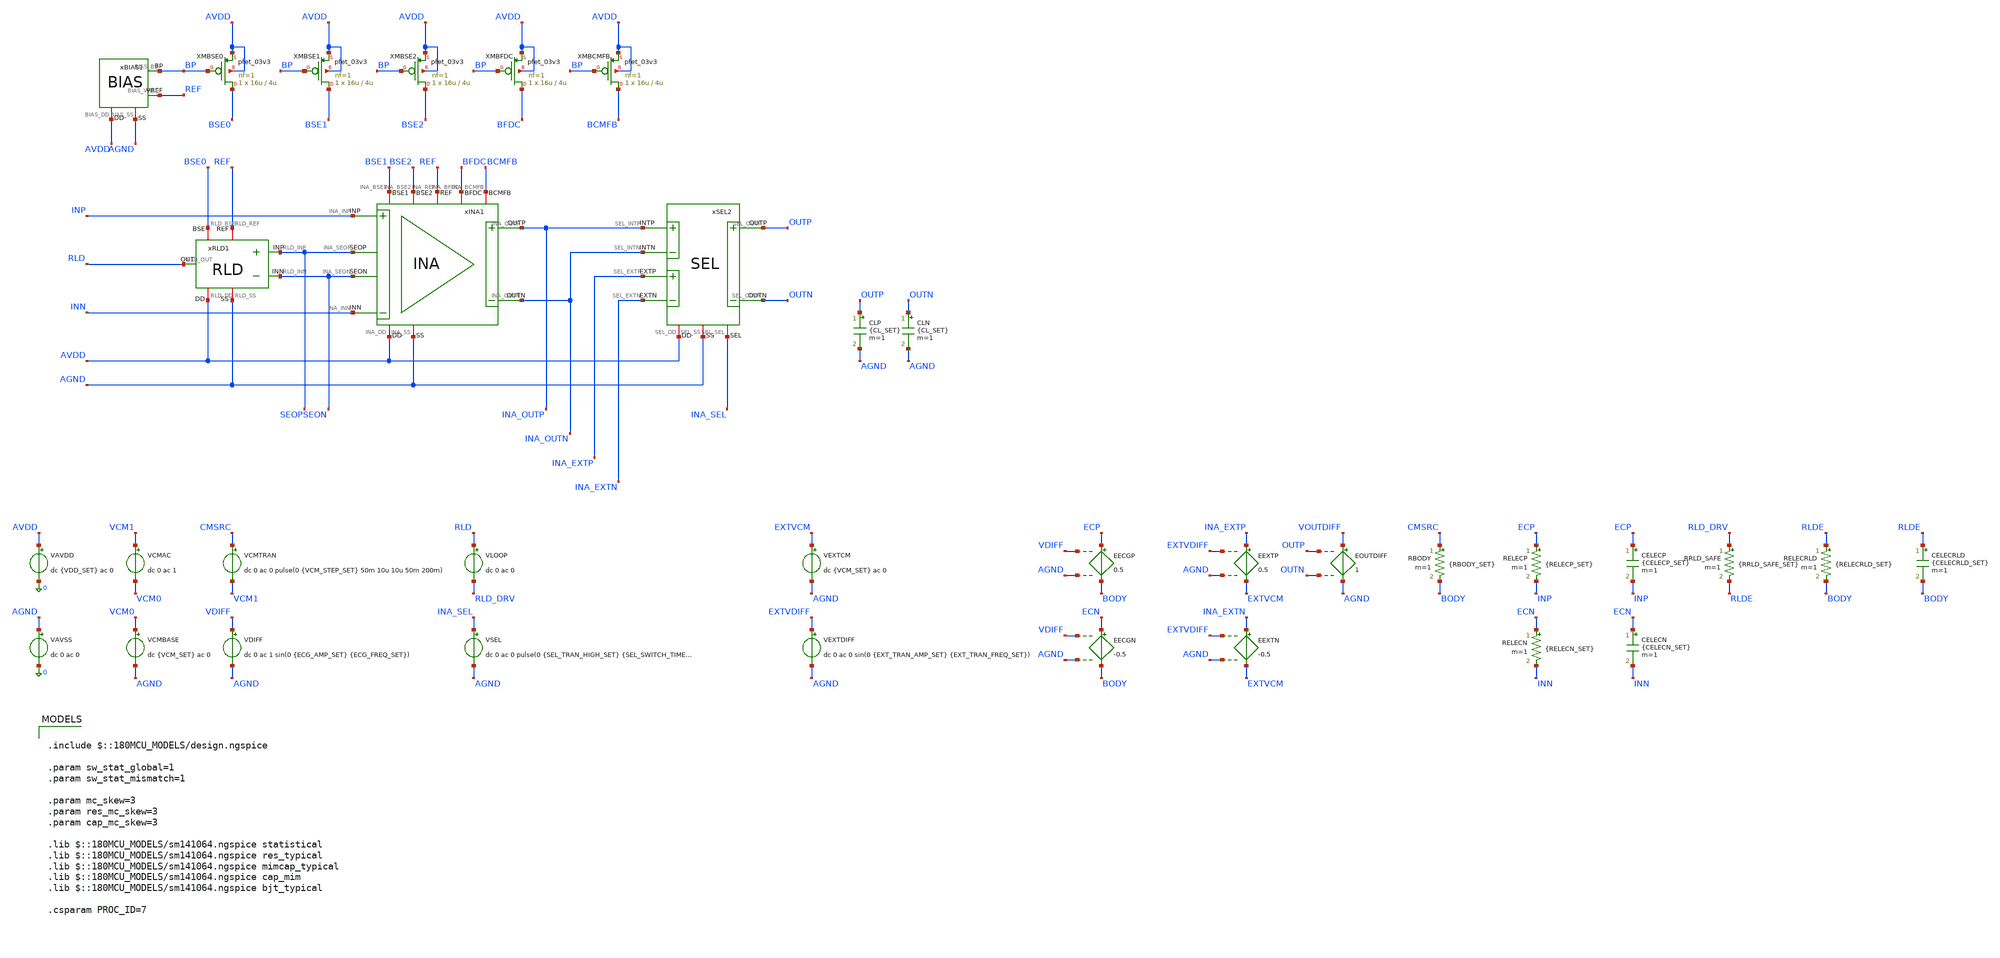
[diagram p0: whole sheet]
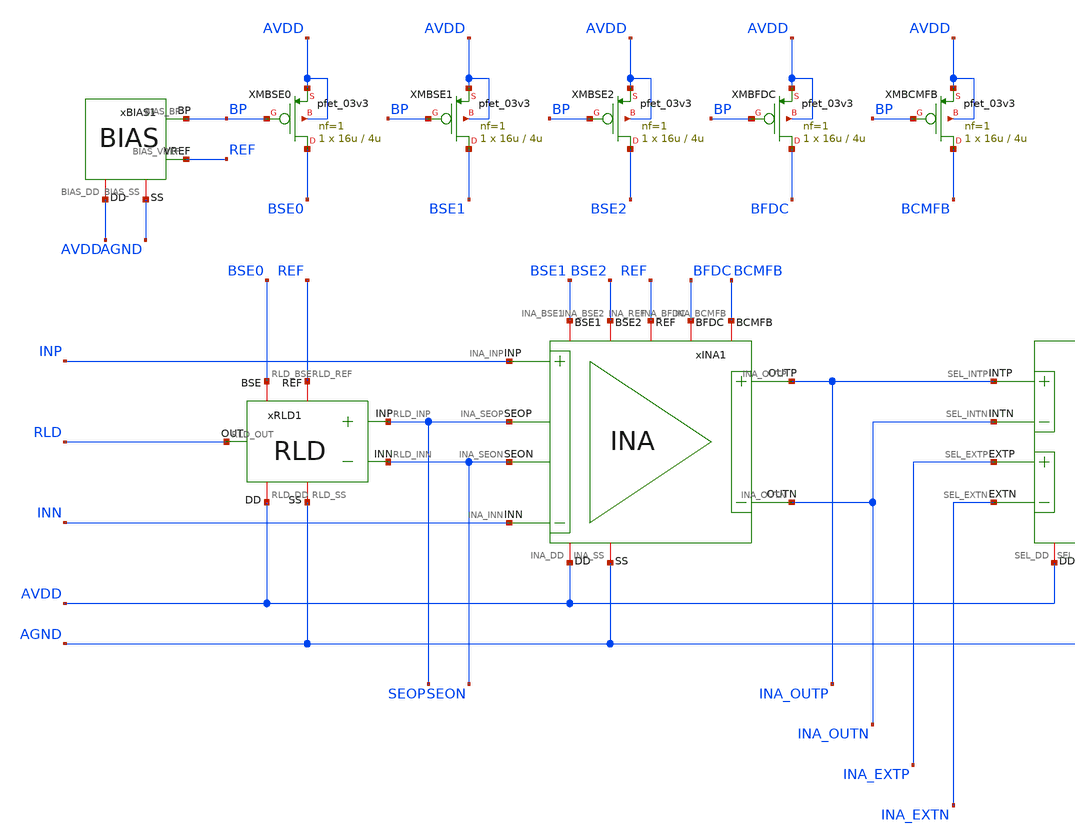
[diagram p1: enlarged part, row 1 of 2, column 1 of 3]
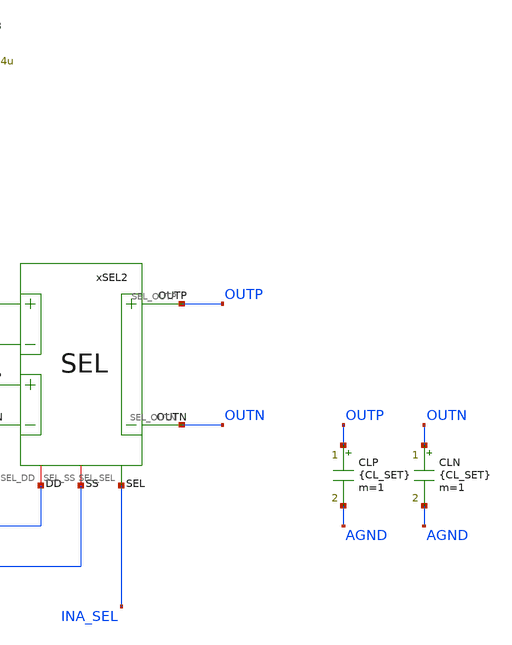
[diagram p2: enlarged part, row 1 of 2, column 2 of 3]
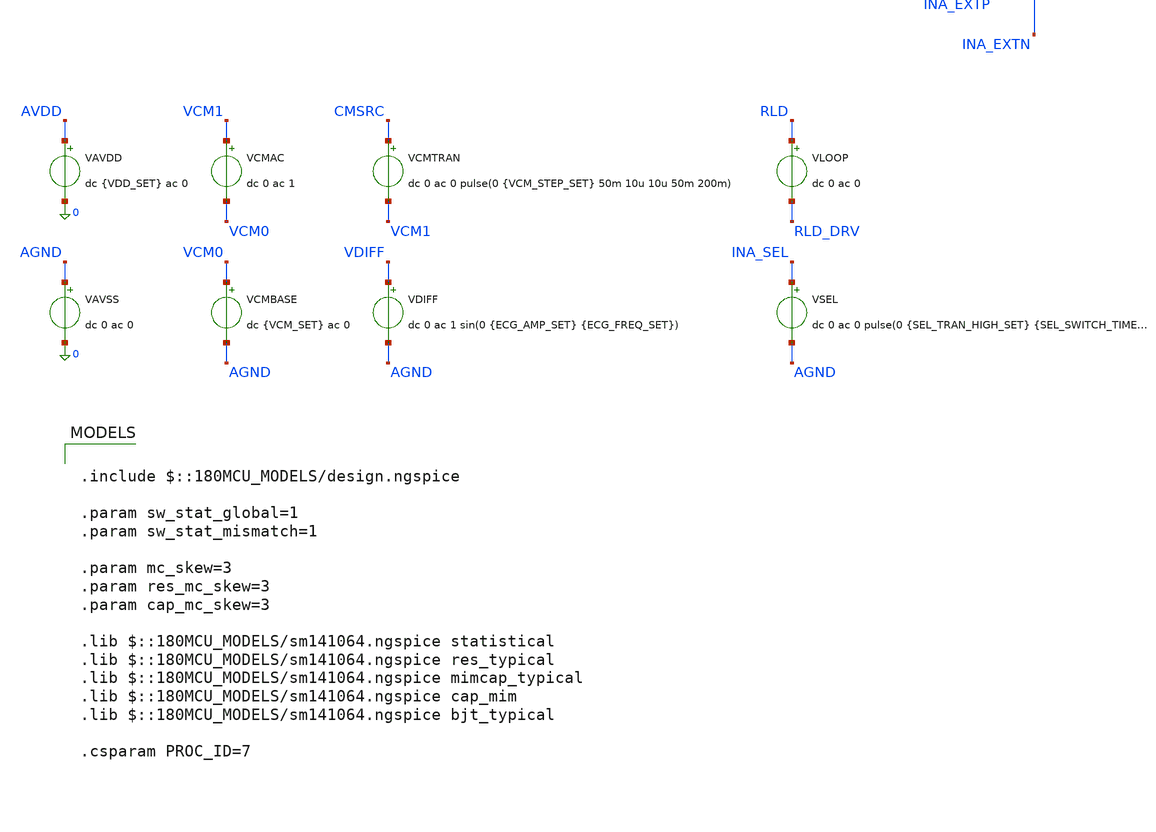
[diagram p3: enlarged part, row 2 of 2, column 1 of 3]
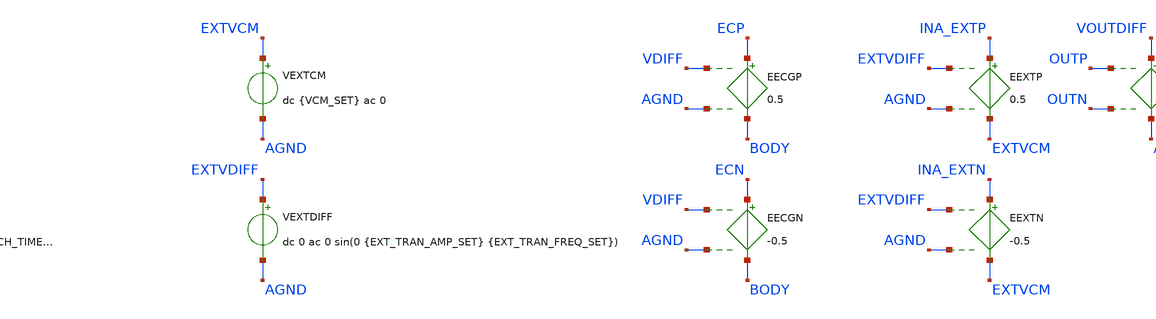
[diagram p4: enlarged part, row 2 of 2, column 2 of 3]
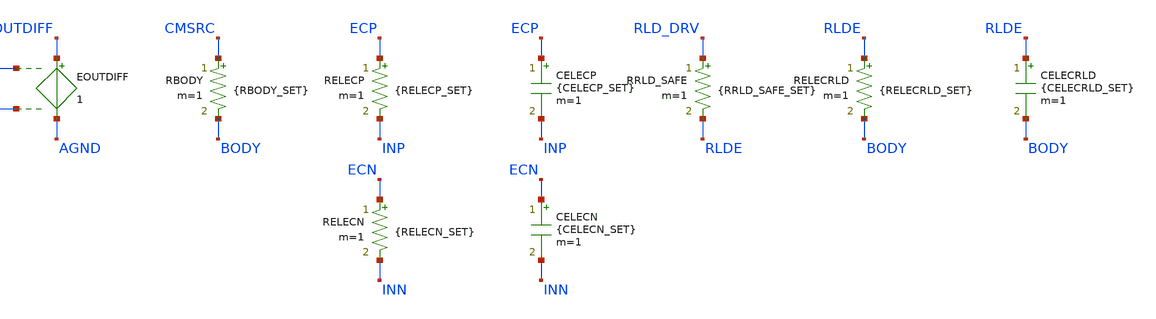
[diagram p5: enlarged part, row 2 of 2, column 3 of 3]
** sch_path: Design_Files/IC Design/Testbench/INA_RLD/INA_RLD_TB_FULL.sch
**.subckt INA_RLD_TB_FULL
xSEL2 AVDD AGND INA_OUTP INA_OUTN OUTN OUTP INA_EXTP INA_EXTN INA_SEL SEL
xINA1 AVDD AGND INP INN INA_OUTN BFDC INA_OUTP BCMFB REF SEON SEOP BSE1 BSE2 INA
xRLD1 AVDD AGND SEOP SEON RLD REF BSE0 RLD
CLP OUTP AGND {CL_SET} m=1
CLN OUTN AGND {CL_SET} m=1
xBIAS1 AVDD AGND BP REF BIAS
XMBSE0 BSE0 BP AVDD AVDD pfet_03v3 L=4u W=16u nf=1 ad='int((nf+1)/2) * W/nf * 0.18u' as='int((nf+2)/2) * W/nf * 0.18u'
+ pd='2*int((nf+1)/2) * (W/nf + 0.18u)' ps='2*int((nf+2)/2) * (W/nf + 0.18u)' nrd='0.18u / W' nrs='0.18u / W'
+ sa=0 sb=0 sd=0 m=1
XMBSE1 BSE1 BP AVDD AVDD pfet_03v3 L=4u W=16u nf=1 ad='int((nf+1)/2) * W/nf * 0.18u' as='int((nf+2)/2) * W/nf * 0.18u'
+ pd='2*int((nf+1)/2) * (W/nf + 0.18u)' ps='2*int((nf+2)/2) * (W/nf + 0.18u)' nrd='0.18u / W' nrs='0.18u / W'
+ sa=0 sb=0 sd=0 m=1
XMBSE2 BSE2 BP AVDD AVDD pfet_03v3 L=4u W=16u nf=1 ad='int((nf+1)/2) * W/nf * 0.18u' as='int((nf+2)/2) * W/nf * 0.18u'
+ pd='2*int((nf+1)/2) * (W/nf + 0.18u)' ps='2*int((nf+2)/2) * (W/nf + 0.18u)' nrd='0.18u / W' nrs='0.18u / W'
+ sa=0 sb=0 sd=0 m=1
XMBFDC BFDC BP AVDD AVDD pfet_03v3 L=4u W=16u nf=1 ad='int((nf+1)/2) * W/nf * 0.18u' as='int((nf+2)/2) * W/nf * 0.18u'
+ pd='2*int((nf+1)/2) * (W/nf + 0.18u)' ps='2*int((nf+2)/2) * (W/nf + 0.18u)' nrd='0.18u / W' nrs='0.18u / W'
+ sa=0 sb=0 sd=0 m=1
XMBCMFB BCMFB BP AVDD AVDD pfet_03v3 L=4u W=16u nf=1 ad='int((nf+1)/2) * W/nf * 0.18u' as='int((nf+2)/2) * W/nf * 0.18u'
+ pd='2*int((nf+1)/2) * (W/nf + 0.18u)' ps='2*int((nf+2)/2) * (W/nf + 0.18u)' nrd='0.18u / W' nrs='0.18u / W'
+ sa=0 sb=0 sd=0 m=1
VAVDD AVDD 0 dc {VDD_SET} ac 0
.save i(vavdd)
VCMBASE VCM0 AGND dc {VCM_SET} ac 0
VCMAC VCM1 VCM0 dc 0 ac 1
VAVSS AGND 0 dc 0 ac 0
VCMTRAN CMSRC VCM1 dc 0 ac 0 pulse(0 {VCM_STEP_SET} 50m 10u 10u 50m 200m)
EECGP ECP BODY VDIFF AGND 0.5
EECGN ECN BODY VDIFF AGND -0.5
EEXTP INA_EXTP EXTVCM EXTVDIFF AGND 0.5
VDIFF VDIFF AGND dc 0 ac 1 sin(0 {ECG_AMP_SET} {ECG_FREQ_SET})
VLOOP RLD RLD_DRV dc 0 ac 0
.save i(vloop)
VSEL INA_SEL AGND dc 0 ac 0 pulse(0 {SEL_TRAN_HIGH_SET} {SEL_SWITCH_TIME_SET} 1u 1u 400m 800m)
VEXTCM EXTVCM AGND dc {VCM_SET} ac 0
VEXTDIFF EXTVDIFF AGND dc 0 ac 0 sin(0 {EXT_TRAN_AMP_SET} {EXT_TRAN_FREQ_SET})
EEXTN INA_EXTN EXTVCM EXTVDIFF AGND -0.5
EOUTDIFF VOUTDIFF AGND OUTP OUTN 1
RBODY CMSRC BODY {RBODY_SET} m=1
RELECP ECP INP {RELECP_SET} m=1
RELECN ECN INN {RELECN_SET} m=1
CELECP ECP INP {CELECP_SET} m=1
CELECN ECN INN {CELECN_SET} m=1
RRLD_SAFE RLD_DRV RLDE {RRLD_SAFE_SET} m=1
RELECRLD RLDE BODY {RELECRLD_SET} m=1
CELECRLD RLDE BODY {CELECRLD_SET} m=1
**** begin user architecture code

.include $::180MCU_MODELS/design.ngspice

.param sw_stat_global=1
.param sw_stat_mismatch=1

.param mc_skew=3
.param res_mc_skew=3
.param cap_mc_skew=3

.lib $::180MCU_MODELS/sm141064.ngspice statistical
.lib $::180MCU_MODELS/sm141064.ngspice res_typical
.lib $::180MCU_MODELS/sm141064.ngspice mimcap_typical
.lib $::180MCU_MODELS/sm141064.ngspice cap_mim
.lib $::180MCU_MODELS/sm141064.ngspice bjt_typical

.csparam PROC_ID=7



.param VDD_SET=3.3
.param TEMP_SET=27
.param VCM_SET={VDD_SET/2}

.param CL_SET=10p

.param ECG_AMP_SET=0.5m
.param ECG_FREQ_SET=10
.param VCM_STEP_SET=300m

.param RBODY_SET=100Meg

.param RELECP_SET=100k
.param RELECN_SET=100k
.param CELECP_SET=100n
.param CELECN_SET=100n

.param RRLD_SAFE_SET=1Meg
.param RELECRLD_SET=100k
.param CELECRLD_SET=100n

.param SEL_TRAN_HIGH_SET=0
.param SEL_SWITCH_TIME_SET=200m
.param EXT_TRAN_AMP_SET=0
.param EXT_TRAN_FREQ_SET=25

.csparam MC_RUNS=200

.temp {TEMP_SET}

.options gmin=1e-12
.options rshunt=1e12
.options method=gear





.control

destroy all

set noaskquit
set wr_singlescale
unset wr_vecnames

option klu
option numdgt=15
option method=gear
option maxord=2
option plotwinsize=0

if $&PROC_ID = 5
set proc=MM
else
if $&PROC_ID = 6
set proc=GL
else
set proc=FULL
end
end

shell mkdir -p /foss/designs/ECG_Acquisition_IC/Measurement_Results/IC_Simulation/INA_RLD/{$proc}.Result_txt
shell rm -f /foss/designs/ECG_Acquisition_IC/Measurement_Results/IC_Simulation/INA_RLD/{$proc}.Result_txt/{$proc}.mc_summary.txt

echo run vos_in_V out_cm_error_V rld_dc_error_V idd_A power_W s1_gain s2_gain ina_gain ina_gain_error_pct
+ ina_gain_150 rld_ugf_Hz rld_pm_deg > /foss/designs/ECG_Acquisition_IC/Measurement_Results/IC_Simulation/INA_RLD/{$proc}.Result_txt/{$proc}.mc_summary.txt

let run=1
let mc_runs=$&MC_RUNS

dowhile run <= mc_runs

set runnum=$&run

setseed $runnum
mc_source

option klu
option numdgt=15
option method=gear
option maxord=2
option plotwinsize=0

save all

alter RELECP 100k
alter RELECN 100k
alter CELECP 100n
alter CELECN 100n
alter RRLD_SAFE 1Meg

alter @VSEL[DC]=0
alter @VDIFF[ACMAG]=0
alter @VCMAC[ACMAG]=0
alter @VLOOP[ACMAG]=0
alter @VEXTDIFF[ACMAG]=0


* OP

op

let ina_offset_out=v(INA_OUTP)-v(INA_OUTN)
let out_cm=0.5*(v(OUTP)+v(OUTN))-v(AGND)
let out_cm_error=out_cm-(v(REF)-v(AGND))
let rld_dc_error=v(RLD)-v(REF)
let idd_total=abs(vavdd#branch)
let power_total=(v(AVDD)-v(AGND))*idd_total

set ina_offset_out_val=$&ina_offset_out
set out_cm_error_val=$&out_cm_error
set rld_dc_error_val=$&rld_dc_error
set idd_val=$&idd_total
set power_val=$&power_total

destroy all


* INA AC

alter RRLD_SAFE 1Meg
alter @VSEL[DC]=0
alter @VDIFF[ACMAG]=1
alter @VDIFF[ACPHASE]=0
alter @VCMAC[ACMAG]=0
alter @VLOOP[ACMAG]=0
alter @VEXTDIFF[ACMAG]=0

ac dec 100 0.1 1Meg

let vin_diff=v(INP)-v(INN)
let se_diff=v(SEOP)-v(SEON)
let ina_diff=v(INA_OUTP)-v(INA_OUTN)

let s1_gain=mag(se_diff/vin_diff)
let s2_gain=mag(ina_diff/se_diff)
let ina_gain=mag(ina_diff/vin_diff)

meas ac s1_gain_10 find s1_gain at=10
meas ac s2_gain_10 find s2_gain at=10
meas ac ina_gain_10 find ina_gain at=10
meas ac ina_gain_150 find ina_gain at=150

let ina_gain_error_pct=100*(ina_gain_10/240-1)
let vos_in=$ina_offset_out_val/ina_gain_10

set vos_val=$&vos_in
set s1_val=$&s1_gain_10
set s2_val=$&s2_gain_10
set ina_val=$&ina_gain_10
set ina_err_val=$&ina_gain_error_pct
set ina150_val=$&ina_gain_150

destroy all


* RLD LOOP

alter RRLD_SAFE 1Meg
alter @VSEL[DC]=0
alter @VDIFF[ACMAG]=0
alter @VCMAC[ACMAG]=0
alter @VLOOP[ACMAG]=1
alter @VLOOP[ACPHASE]=0
alter @VEXTDIFF[ACMAG]=0

ac dec 100 0.1 100k

let loop_in=v(RLD_DRV)-v(AGND)
let loop_out=v(RLD)-v(AGND)

let loop_tf=-loop_out/loop_in
let loop_mag=mag(loop_tf)
let loop_phase=(180/3.141592653589793)*cph(loop_tf)

meas ac rld_ugf when loop_mag=1 cross=1
meas ac rld_phase find loop_phase at=$&rld_ugf

let rld_pm=180+rld_phase

set ugf_val=$&rld_ugf
set pm_val=$&rld_pm

echo $runnum $vos_val $out_cm_error_val $rld_dc_error_val $idd_val $power_val $s1_val $s2_val $ina_val
+ $ina_err_val $ina150_val $ugf_val $pm_val >> /foss/designs/ECG_Acquisition_IC/Measurement_Results/IC_Simulation/INA_RLD/{$proc}.Result_txt/{$proc}.mc_summary.txt

destroy all

let run=run+1

end

quit

.endc


**** end user architecture code
**.ends
.end
